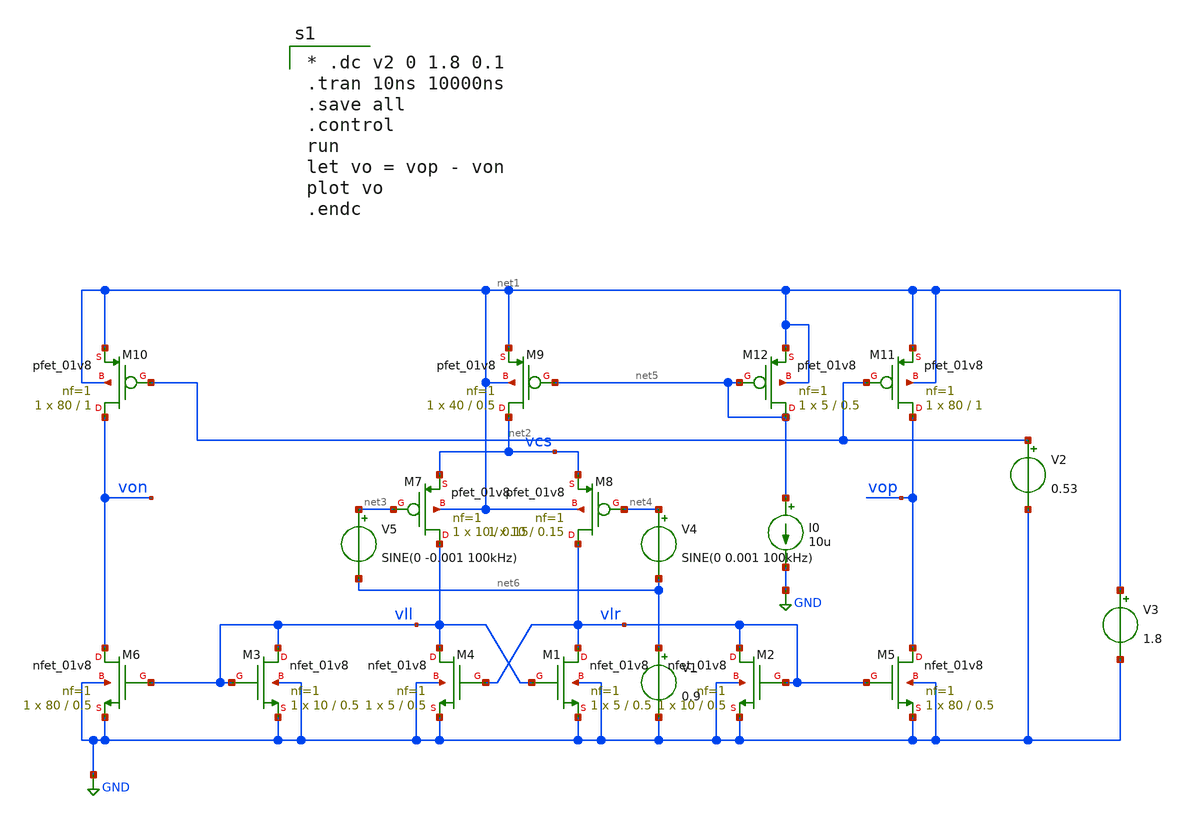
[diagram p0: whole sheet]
** sch_path: xschem/diffamp_current_trantb.sch
**.subckt diffamp_current_trantb
XM1 vlr vll GND GND sky130_fd_pr__nfet_01v8 L=0.5 W=5 nf=1 ad='int((nf+1)/2) * W/nf * 0.29' as='int((nf+2)/2) * W/nf * 0.29'
+ pd='2*int((nf+1)/2) * (W/nf + 0.29)' ps='2*int((nf+2)/2) * (W/nf + 0.29)' nrd='0.29 / W' nrs='0.29 / W'
+ sa=0 sb=0 sd=0 mult=1 m=1
XM3 vll vll GND GND sky130_fd_pr__nfet_01v8 L=0.5 W=10 nf=1 ad='int((nf+1)/2) * W/nf * 0.29' as='int((nf+2)/2) * W/nf * 0.29'
+ pd='2*int((nf+1)/2) * (W/nf + 0.29)' ps='2*int((nf+2)/2) * (W/nf + 0.29)' nrd='0.29 / W' nrs='0.29 / W'
+ sa=0 sb=0 sd=0 mult=1 m=1
XM2 vlr vlr GND GND sky130_fd_pr__nfet_01v8 L=0.5 W=10 nf=1 ad='int((nf+1)/2) * W/nf * 0.29' as='int((nf+2)/2) * W/nf * 0.29'
+ pd='2*int((nf+1)/2) * (W/nf + 0.29)' ps='2*int((nf+2)/2) * (W/nf + 0.29)' nrd='0.29 / W' nrs='0.29 / W'
+ sa=0 sb=0 sd=0 mult=1 m=1
XM4 vll vlr GND GND sky130_fd_pr__nfet_01v8 L=0.5 W=5 nf=1 ad='int((nf+1)/2) * W/nf * 0.29' as='int((nf+2)/2) * W/nf * 0.29'
+ pd='2*int((nf+1)/2) * (W/nf + 0.29)' ps='2*int((nf+2)/2) * (W/nf + 0.29)' nrd='0.29 / W' nrs='0.29 / W'
+ sa=0 sb=0 sd=0 mult=1 m=1
XM5 vop vlr GND GND sky130_fd_pr__nfet_01v8 L=0.5 W=80 nf=1 ad='int((nf+1)/2) * W/nf * 0.29' as='int((nf+2)/2) * W/nf * 0.29'
+ pd='2*int((nf+1)/2) * (W/nf + 0.29)' ps='2*int((nf+2)/2) * (W/nf + 0.29)' nrd='0.29 / W' nrs='0.29 / W'
+ sa=0 sb=0 sd=0 mult=1 m=1
XM6 von vll GND GND sky130_fd_pr__nfet_01v8 L=0.5 W=80 nf=1 ad='int((nf+1)/2) * W/nf * 0.29' as='int((nf+2)/2) * W/nf * 0.29'
+ pd='2*int((nf+1)/2) * (W/nf + 0.29)' ps='2*int((nf+2)/2) * (W/nf + 0.29)' nrd='0.29 / W' nrs='0.29 / W'
+ sa=0 sb=0 sd=0 mult=1 m=1
XM7 vll net3 vcs net1 sky130_fd_pr__pfet_01v8 L=0.15 W=10 nf=1 ad='int((nf+1)/2) * W/nf * 0.29' as='int((nf+2)/2) * W/nf * 0.29'
+ pd='2*int((nf+1)/2) * (W/nf + 0.29)' ps='2*int((nf+2)/2) * (W/nf + 0.29)' nrd='0.29 / W' nrs='0.29 / W'
+ sa=0 sb=0 sd=0 mult=1 m=1
XM8 vlr net4 vcs net1 sky130_fd_pr__pfet_01v8 L=0.15 W=10 nf=1 ad='int((nf+1)/2) * W/nf * 0.29' as='int((nf+2)/2) * W/nf * 0.29'
+ pd='2*int((nf+1)/2) * (W/nf + 0.29)' ps='2*int((nf+2)/2) * (W/nf + 0.29)' nrd='0.29 / W' nrs='0.29 / W'
+ sa=0 sb=0 sd=0 mult=1 m=1
XM9 vcs net5 net1 net1 sky130_fd_pr__pfet_01v8 L=0.5 W=40 nf=1 ad='int((nf+1)/2) * W/nf * 0.29' as='int((nf+2)/2) * W/nf * 0.29'
+ pd='2*int((nf+1)/2) * (W/nf + 0.29)' ps='2*int((nf+2)/2) * (W/nf + 0.29)' nrd='0.29 / W' nrs='0.29 / W'
+ sa=0 sb=0 sd=0 mult=1 m=1
XM10 von net2 net1 net1 sky130_fd_pr__pfet_01v8 L=1 W=80 nf=1 ad='int((nf+1)/2) * W/nf * 0.29' as='int((nf+2)/2) * W/nf * 0.29'
+ pd='2*int((nf+1)/2) * (W/nf + 0.29)' ps='2*int((nf+2)/2) * (W/nf + 0.29)' nrd='0.29 / W' nrs='0.29 / W'
+ sa=0 sb=0 sd=0 mult=1 m=1
XM11 vop net2 net1 net1 sky130_fd_pr__pfet_01v8 L=1 W=80 nf=1 ad='int((nf+1)/2) * W/nf * 0.29' as='int((nf+2)/2) * W/nf * 0.29'
+ pd='2*int((nf+1)/2) * (W/nf + 0.29)' ps='2*int((nf+2)/2) * (W/nf + 0.29)' nrd='0.29 / W' nrs='0.29 / W'
+ sa=0 sb=0 sd=0 mult=1 m=1
V1 net6 GND 0.9
XM12 net5 net5 net1 net1 sky130_fd_pr__pfet_01v8 L=0.5 W=5 nf=1 ad='int((nf+1)/2) * W/nf * 0.29' as='int((nf+2)/2) * W/nf * 0.29'
+ pd='2*int((nf+1)/2) * (W/nf + 0.29)' ps='2*int((nf+2)/2) * (W/nf + 0.29)' nrd='0.29 / W' nrs='0.29 / W'
+ sa=0 sb=0 sd=0 mult=1 m=1
I0 net5 GND 10u
V2 net2 GND 0.53
V3 net1 GND 1.8
V4 net4 net6 SINE(0 0.001 100kHz)
V5 net3 net6 SINE(0 -0.001 100kHz)
**** begin user architecture code
.lib $::SKYWATER_MODELS/sky130.lib.spice tt
.include $::PDKPATH/libs.ref/sky130_fd_sc_hs/spice/sky130_fd_sc_hs.spice


* .dc v2 0 1.8 0.1
.tran 10ns 10000ns
.save all
.control
run
let vo = vop - von
plot vo
.endc


**** end user architecture code
**.ends
.GLOBAL GND
.end
